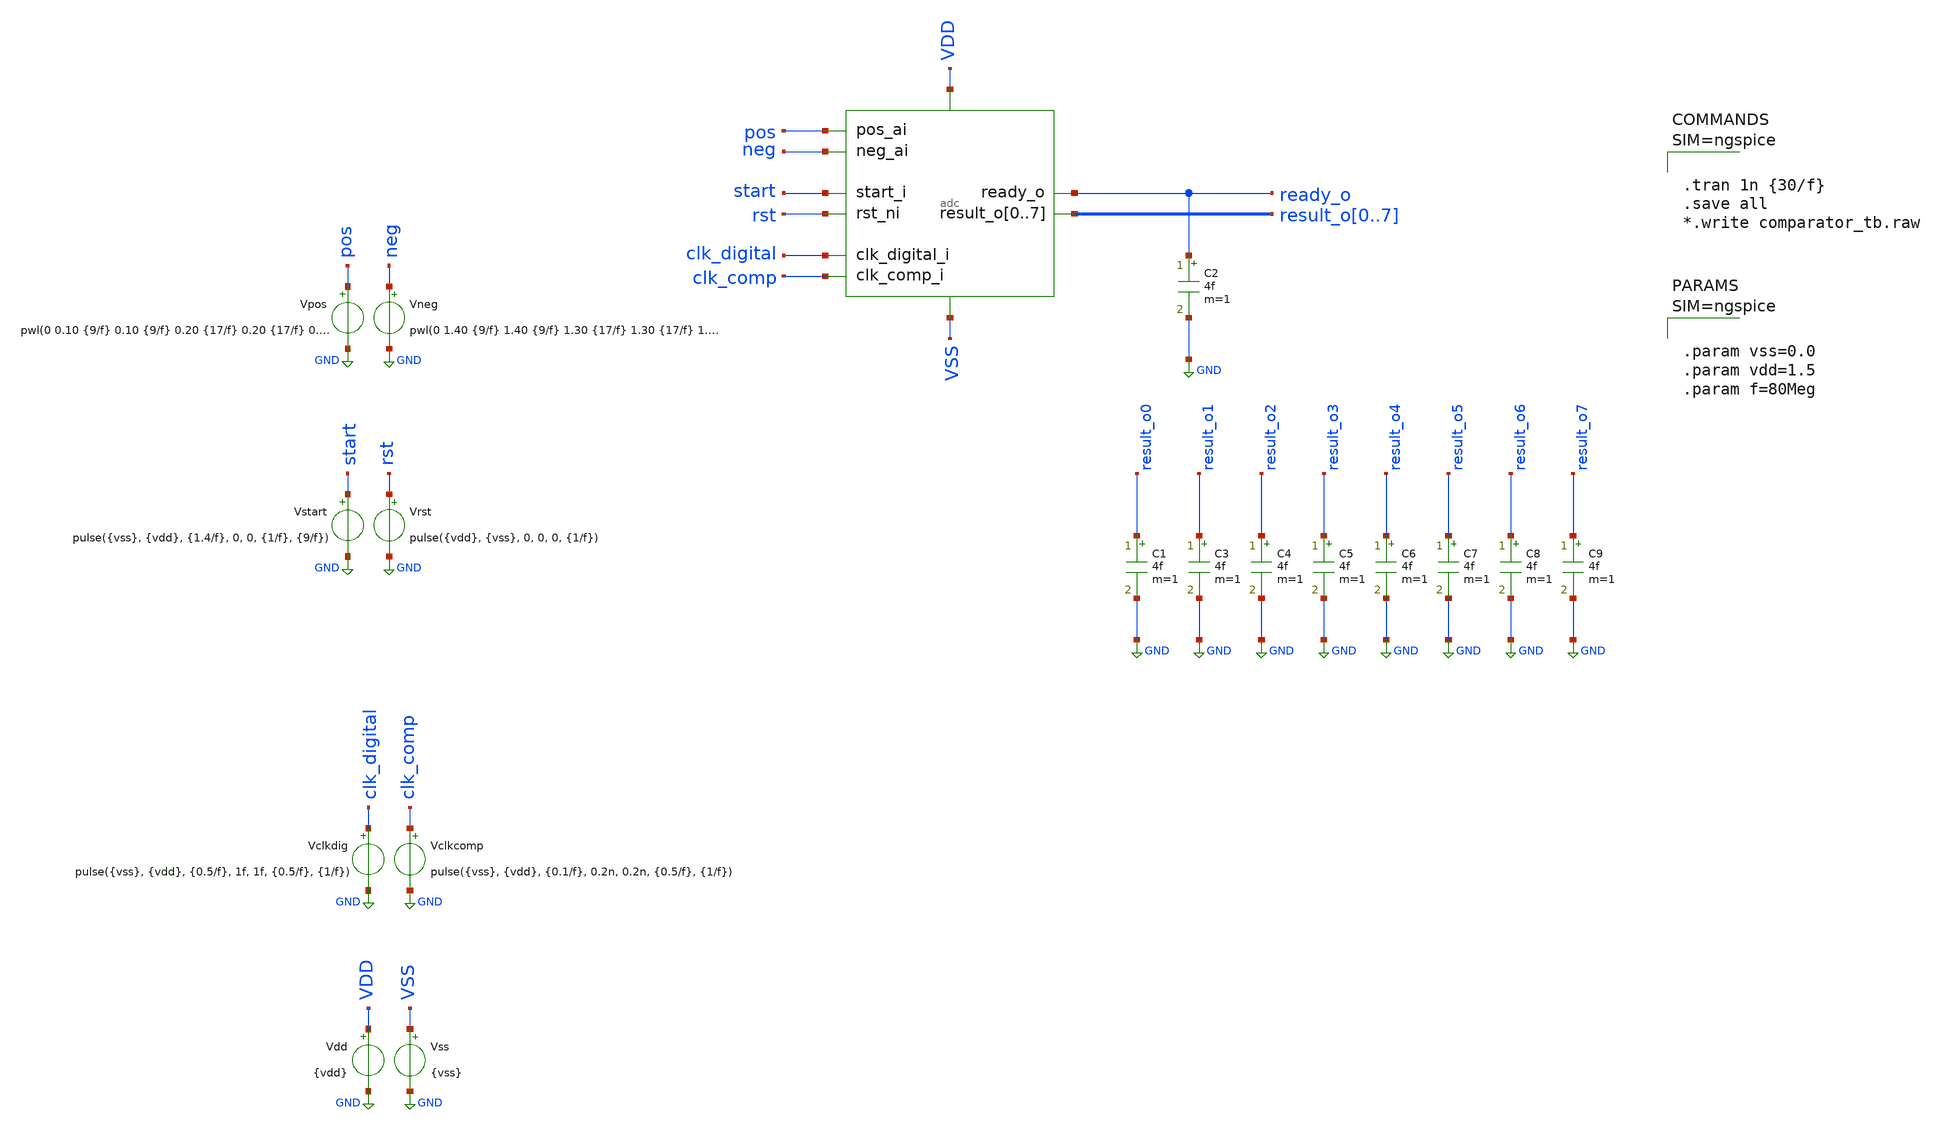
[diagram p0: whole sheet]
** sch_path: designs/diff_9cycle/xschem/adc_tb.sch
**.subckt adc_tb
x1 pos start rst clk_digital result_o0 result_o1 result_o2 result_o3 result_o4 result_o5 result_o6
+ result_o7 ready_o VDD VSS clk_comp neg adc
Vclkdig clk_digital GND pulse({vss}, {vdd}, {0.5/f}, 1f, 1f, {0.5/f}, {1/f})
Vrst rst GND pulse({vdd}, {vss}, 0, 0, 0, {1/f})
Vstart start GND pulse({vss}, {vdd}, {1.4/f}, 0, 0, {1/f}, {9/f})
Vpos pos GND pwl(0 0.10 {9/f} 0.10 {9/f} 0.20 {17/f} 0.20 {17/f} 0.30 {25/f} 0.30 {25/f} 0.40 {33/f}
+ 0.40 {33/f} 0.50 {41/f} 0.50 {41/f} 0.60 {49/f} 0.60 {49/f} 0.70 {57/f} 0.70 {57/f} 0.80 {65/f} 0.80
+ {65/f} 0.90 {73/f} 0.90 {73/f} 1.00 {81/f} 1.00 {81/f} 1.10 {89/f} 1.10 {89/f} 1.20 {97/f} 1.20 {97/f}
+ 1.30 {105/f} 1.30 {105/f} 1.40 {113/f} 1.40)
.save i(vpos)
Vdd VDD GND {vdd}
Vss VSS GND {vss}
C1 result_o0 GND 4f m=1
C2 ready_o GND 4f m=1
C3 result_o1 GND 4f m=1
C4 result_o2 GND 4f m=1
C5 result_o3 GND 4f m=1
Vclkcomp clk_comp GND pulse({vss}, {vdd}, {0.1/f}, 0.2n, 0.2n, {0.5/f}, {1/f})
C6 result_o4 GND 4f m=1
C7 result_o5 GND 4f m=1
C8 result_o6 GND 4f m=1
C9 result_o7 GND 4f m=1
Vneg neg GND pwl(0 1.40 {9/f} 1.40 {9/f} 1.30 {17/f} 1.30 {17/f} 1.20 {25/f} 1.20 {25/f} 1.10 {33/f}
+ 1.10 {33/f} 1.00 {41/f} 1.00 {41/f} 0.90 {49/f} 0.90 {49/f} 0.80 {57/f} 0.80 {57/f} 0.70 {65/f} 0.70
+ {65/f} 0.60 {73/f} 0.60 {73/f} 0.50 {81/f} 0.50 {81/f} 0.40 {89/f} 0.40 {89/f} 0.30 {97/f} 0.30 {97/f}
+ 0.20 {105/f} 0.20 {105/f} 0.10 {113/f} 0.10)
.save i(vneg)
**** begin user architecture code

.lib $::SG13G2_MODELS/cornerMOSlv.lib mos_tt
.lib $::SG13G2_MODELS/cornerCAP.lib cap_typ
.include $::PDK_ROOT/ihp-sg13g2/libs.ref/sg13g2_stdcell/spice/sg13g2_stdcell.spice




.tran 1n {30/f}
.save all
*.write comparator_tb.raw






.param vss=0.0
.param vdd=1.5
.param f=80Meg






.control
pre_set auto_bridge_d_out =  ( ".model auto_bridge_out bidi_bridge(direction=0 out_high=1.5
+ t_rise=0.2n t_fall=0.2n)"    "auto_bridge_out%d [ %s ] [ %s ] null auto_bridge_out" )
pre_set auto_bridge_d_in =  ( ".model auto_bridge_in bidi_bridge(direction=1 in_low=0.5 in_high=1)"
+    "auto_bridge_in%d [ %s ] [ %s ] null auto_bridge_in" )
.endc



**** end user architecture code
**.ends
.GLOBAL GND
.end
